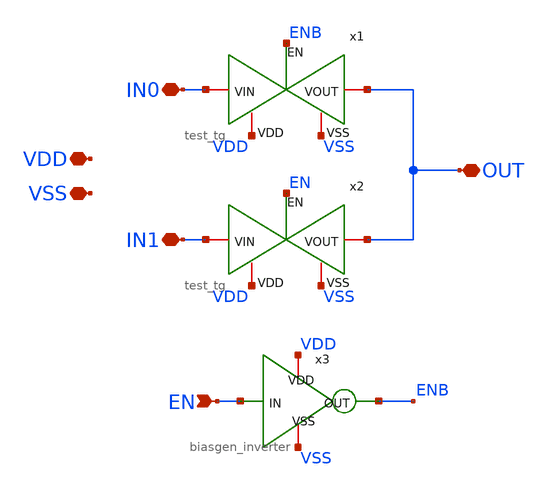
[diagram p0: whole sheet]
** sch_path: designs/libs/core_top/top_amux_2x1/top_amux_2x1.sch
**.subckt top_amux_2x1 VDD VSS EN IN0 IN1 OUT
*.iopin VDD
*.iopin VSS
*.ipin EN
*.iopin IN0
*.iopin IN1
*.iopin OUT
x1 VDD ENB IN0 OUT VSS test_tg
x2 VDD EN IN1 OUT VSS test_tg
x3 VDD EN ENB VSS biasgen_inverter
**.ends

* expanding   symbol:  libs/core_test/test_tg/test_tg.sym # of pins=5
** sym_path: designs/libs/core_test/test_tg/test_tg.sym
** sch_path: designs/libs/core_test/test_tg/test_tg.sch
.subckt test_tg VDD EN VIN VOUT VSS
*.iopin VIN
*.iopin VOUT
*.ipin EN
*.iopin VDD
*.iopin VSS
XM1 VIN EN VOUT VSS nfet_05v0 L=0.60u W=1.5u nf=1 ad='int((nf+1)/2) * W/nf * 0.18u' as='int((nf+2)/2) * W/nf * 0.18u'
+ pd='2*int((nf+1)/2) * (W/nf + 0.18u)' ps='2*int((nf+2)/2) * (W/nf + 0.18u)' nrd='0.18u / W' nrs='0.18u / W'
+ sa=0 sb=0 sd=0 m=2
XM2 VOUT ENB VIN VDD pfet_05v0 L=0.50u W=1.5u nf=1 ad='int((nf+1)/2) * W/nf * 0.18u' as='int((nf+2)/2) * W/nf * 0.18u'
+ pd='2*int((nf+1)/2) * (W/nf + 0.18u)' ps='2*int((nf+2)/2) * (W/nf + 0.18u)' nrd='0.18u / W' nrs='0.18u / W'
+ sa=0 sb=0 sd=0 m=6
x1 VDD ENB EN VSS test_inv
.ends


* expanding   symbol:  libs/core_biasgen/biasgen_inverter/biasgen_inverter.sym # of pins=4
** sym_path: designs/libs/core_biasgen/biasgen_inverter/biasgen_inverter.sym
** sch_path: designs/libs/core_biasgen/biasgen_inverter/biasgen_inverter.sch
.subckt biasgen_inverter VDD IN OUT VSS
*.iopin VDD
*.iopin VSS
*.ipin IN
*.opin OUT
XMINV1 OUT IN VSS VSS nfet_05v0 L=0.60u W=0.50u nf=1 ad='int((nf+1)/2) * W/nf * 0.18u' as='int((nf+2)/2) * W/nf * 0.18u'
+ pd='2*int((nf+1)/2) * (W/nf + 0.18u)' ps='2*int((nf+2)/2) * (W/nf + 0.18u)' nrd='0.18u / W' nrs='0.18u / W'
+ sa=0 sb=0 sd=0 m=1
XMINV2 OUT IN VDD VDD pfet_05v0 L=0.50u W=0.60u nf=1 ad='int((nf+1)/2) * W/nf * 0.18u' as='int((nf+2)/2) * W/nf * 0.18u'
+ pd='2*int((nf+1)/2) * (W/nf + 0.18u)' ps='2*int((nf+2)/2) * (W/nf + 0.18u)' nrd='0.18u / W' nrs='0.18u / W'
+ sa=0 sb=0 sd=0 m=1
.ends


* expanding   symbol:  libs/core_test/test_inv/test_inv.sym # of pins=4
** sym_path: designs/libs/core_test/test_inv/test_inv.sym
** sch_path: designs/libs/core_test/test_inv/test_inv.sch
.subckt test_inv VDD OUT IN VSS
*.opin OUT
*.ipin IN
*.iopin VDD
*.iopin VSS
XM1 OUT IN VSS VSS nfet_05v0 L=0.60u W=0.30u nf=1 ad='int((nf+1)/2) * W/nf * 0.18u' as='int((nf+2)/2) * W/nf * 0.18u'
+ pd='2*int((nf+1)/2) * (W/nf + 0.18u)' ps='2*int((nf+2)/2) * (W/nf + 0.18u)' nrd='0.18u / W' nrs='0.18u / W'
+ sa=0 sb=0 sd=0 m=1
XM2 OUT IN VDD VDD pfet_05v0 L=0.50u W=0.30u nf=2 ad='int((nf+1)/2) * W/nf * 0.18u' as='int((nf+2)/2) * W/nf * 0.18u'
+ pd='2*int((nf+1)/2) * (W/nf + 0.18u)' ps='2*int((nf+2)/2) * (W/nf + 0.18u)' nrd='0.18u / W' nrs='0.18u / W'
+ sa=0 sb=0 sd=0 m=1
.ends

.end
